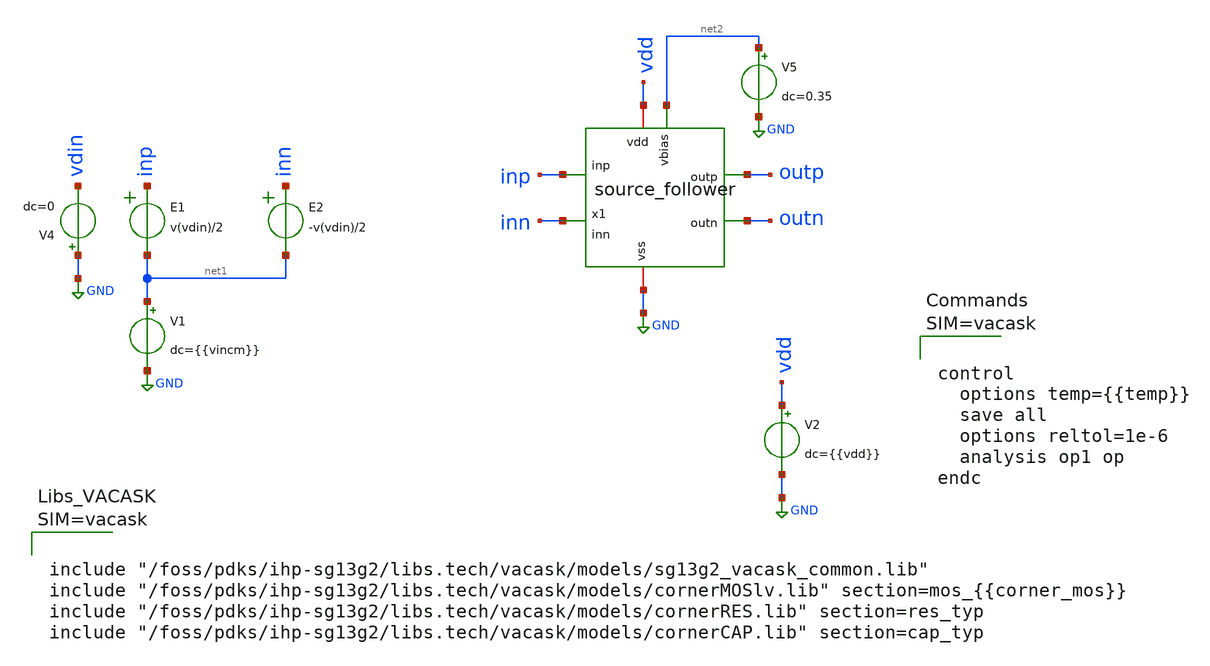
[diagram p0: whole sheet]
** sch_path: examples/source_follower/tb/tb_sf_op_vacask.sch
**.subckt tb_sf_op_vacask
E1 inp net1 VOL=' v(vdin)/2 '
E2 inn net1 VOL=' -v(vdin)/2 '
V1 net1 GND dc={{vincm}}
.save i(v1)
V2 vdd GND dc={{vdd}}
V5 net2 GND dc=0.35
.save i(v5)
V4 GND vdin dc=0
.save i(v4)
x1 vdd inn inp outp outn net2 GND source_follower
**** begin user architecture code






**** end user architecture code
**.ends

* expanding   symbol:  chipify/examples/source_follower/sch/source_follower.sym # of pins=7
** sym_path: examples/source_follower/sch/source_follower.sym
** sch_path: examples/source_follower/sch/source_follower.sch
.subckt source_follower vdd inn inp outp outn vbias vss
*.ipin vbias
*.iopin vdd
*.opin outp
*.iopin vss
*.opin outn
*.ipin inp
*.ipin inn
XM1 outp vbias vss vss sg13_lv_nmos w=100u l=2u ng=20 m=1 mm_ok=1
XM2 vdd inp outp vss sg13_lv_nmos w=200u l=0.13u ng=20 m=1 mm_ok=1
XM3 outn vbias vss vss sg13_lv_nmos w=100u l=2u ng=20 m=1 mm_ok=1
XM4 vdd inn outn vss sg13_lv_nmos w=200u l=0.13u ng=20 m=1 mm_ok=1
.ends

.GLOBAL GND
.end
